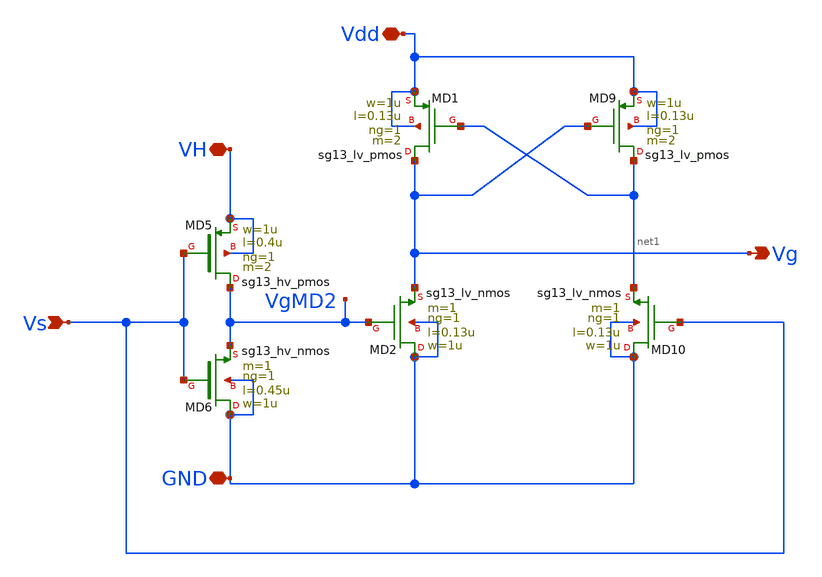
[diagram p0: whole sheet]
** sch_path: xschem/LevelShifter_HL_v1p1.sch
**.subckt LevelShifter_HL_v1p1 VH Vdd Vs Vg GND
*.iopin VH
*.iopin Vdd
*.ipin Vs
*.opin Vg
*.iopin GND
XMD9 net1 Vg Vdd Vdd sg13_lv_pmos w=1u l=0.13u ng=1 m=2 mm_ok=1
XMD10 GND Vs net1 GND sg13_lv_nmos w=1u l=0.13u ng=1 m=1 mm_ok=1
XMD5 VgMD2 Vs VH VH sg13_hv_pmos w=1u l=0.4u ng=1 m=2 mm_ok=1
XMD6 GND Vs VgMD2 GND sg13_hv_nmos w=1u l=0.45u ng=1 m=1 mm_ok=1
XMD1 Vg net1 Vdd Vdd sg13_lv_pmos w=1u l=0.13u ng=1 m=2 mm_ok=1
XMD2 GND VgMD2 Vg GND sg13_lv_nmos w=1u l=0.13u ng=1 m=1 mm_ok=1
**.ends
.end
